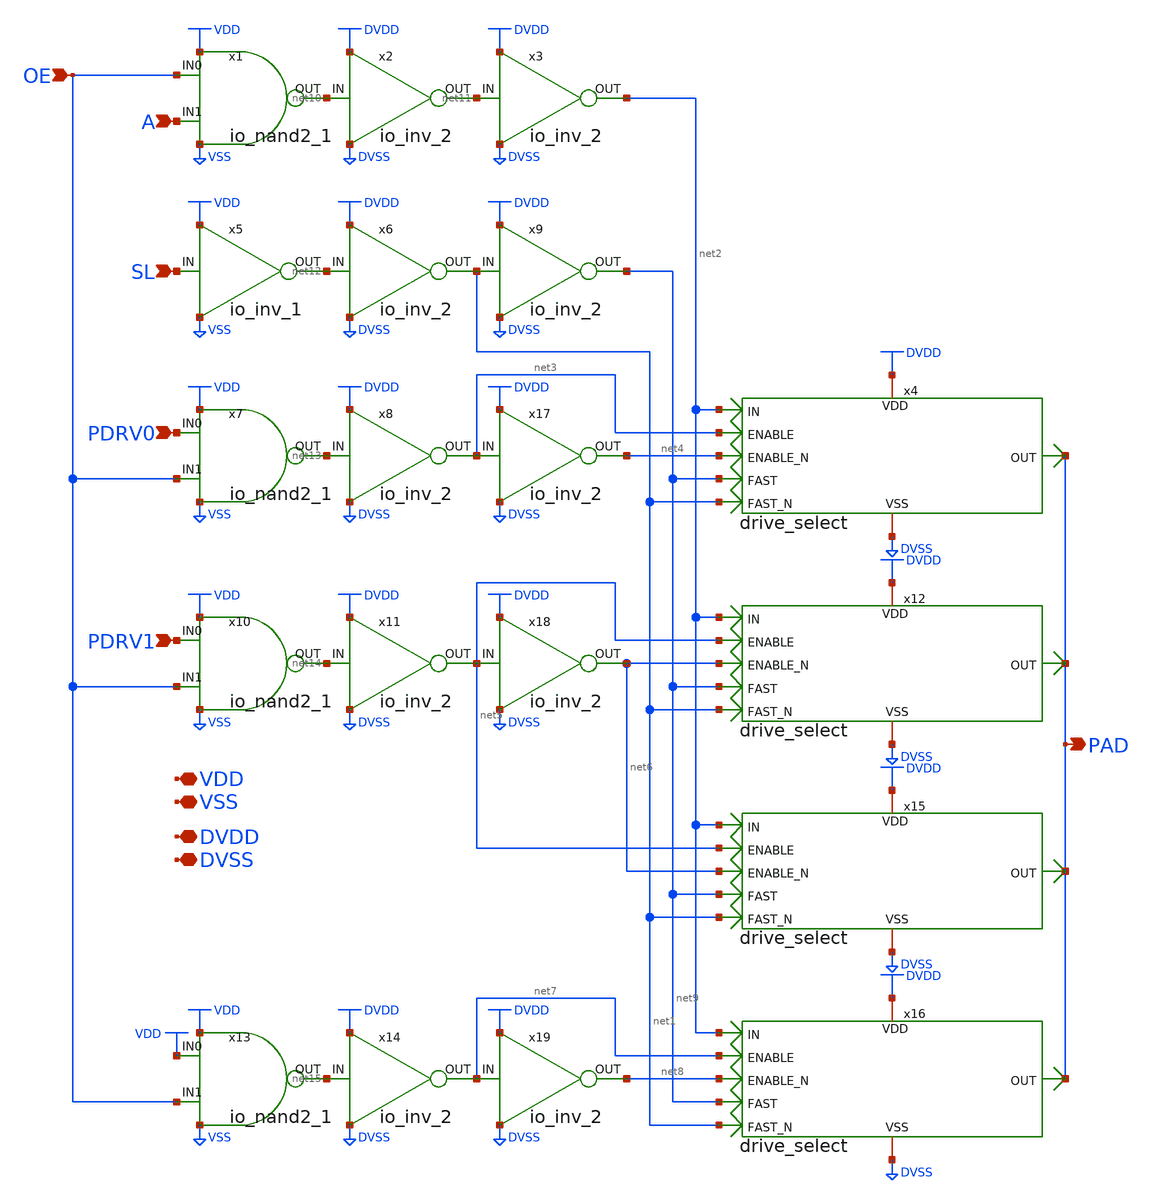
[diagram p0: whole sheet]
** sch_path: io_out.sch
**.subckt io_out OE VDD PAD A SL PDRV0 PDRV1 VSS DVDD DVSS
*.ipin OE
*.iopin VDD
*.opin PAD
*.ipin A
*.ipin SL
*.ipin PDRV0
*.ipin PDRV1
*.iopin VSS
*.iopin DVDD
*.iopin DVSS
x1 OE net10 A VDD VSS io_nand2_1
x2 net10 net11 DVDD DVSS io_inv_2
x3 net11 net2 DVDD DVSS io_inv_2
x4 net1 net2 net3 PAD net9 DVDD DVSS net4 drive_select
x5 SL net12 VDD VSS io_inv_1
x6 net12 net1 DVDD DVSS io_inv_2
x7 PDRV0 net13 OE VDD VSS io_nand2_1
x8 net13 net3 DVDD DVSS io_inv_2
x10 PDRV1 net14 OE VDD VSS io_nand2_1
x11 net14 net5 DVDD DVSS io_inv_2
x13 VDD net15 OE VDD VSS io_nand2_1
x14 net15 net7 DVDD DVSS io_inv_2
x9 net1 net9 DVDD DVSS io_inv_2
x12 net1 net2 net5 PAD net9 DVDD DVSS net6 drive_select
x15 net1 net2 net5 PAD net9 DVDD DVSS net6 drive_select
x16 net1 net2 net7 PAD net9 DVDD DVSS net8 drive_select
x17 net3 net4 DVDD DVSS io_inv_2
x18 net5 net6 DVDD DVSS io_inv_2
x19 net7 net8 DVDD DVSS io_inv_2
**.ends

* expanding   symbol:  io_nand2_1.sym # of pins=5
** sym_path: io_nand2_1.sym
** sch_path: io_nand2_1.sch
.subckt io_nand2_1 IN0 OUT IN1 VDD VSS
*.opin OUT
*.ipin IN0
*.ipin IN1
*.iopin VDD
*.iopin VSS
XM1 OUT IN1 VDD VDD pfet_06v0 L=0.70u W=3u nf=1 ad='int((nf+1)/2) * W/nf * 0.18u' as='int((nf+2)/2) * W/nf * 0.18u'
+ pd='2*int((nf+1)/2) * (W/nf + 0.18u)' ps='2*int((nf+2)/2) * (W/nf + 0.18u)' nrd='0.18u / W' nrs='0.18u / W'
+ sa=0 sb=0 sd=0 m=1
XM2 net1 IN0 VSS VSS nfet_06v0 L=0.70u W=3u nf=1 ad='int((nf+1)/2) * W/nf * 0.18u' as='int((nf+2)/2) * W/nf * 0.18u'
+ pd='2*int((nf+1)/2) * (W/nf + 0.18u)' ps='2*int((nf+2)/2) * (W/nf + 0.18u)' nrd='0.18u / W' nrs='0.18u / W'
+ sa=0 sb=0 sd=0 m=1
XM3 OUT IN1 net1 VSS nfet_06v0 L=0.70u W=3u nf=1 ad='int((nf+1)/2) * W/nf * 0.18u' as='int((nf+2)/2) * W/nf * 0.18u'
+ pd='2*int((nf+1)/2) * (W/nf + 0.18u)' ps='2*int((nf+2)/2) * (W/nf + 0.18u)' nrd='0.18u / W' nrs='0.18u / W'
+ sa=0 sb=0 sd=0 m=1
XM4 OUT IN0 VDD VDD pfet_06v0 L=0.70u W=3u nf=1 ad='int((nf+1)/2) * W/nf * 0.18u' as='int((nf+2)/2) * W/nf * 0.18u'
+ pd='2*int((nf+1)/2) * (W/nf + 0.18u)' ps='2*int((nf+2)/2) * (W/nf + 0.18u)' nrd='0.18u / W' nrs='0.18u / W'
+ sa=0 sb=0 sd=0 m=1
.ends


* expanding   symbol:  io_inv_2.sym # of pins=4
** sym_path: io_inv_2.sym
** sch_path: io_inv_2.sch
.subckt io_inv_2 IN OUT VDD VSS
*.opin OUT
*.ipin IN
*.iopin VDD
*.iopin VSS
XM1 OUT IN VDD VDD pfet_06v0 L=0.70u W=6u nf=1 ad='int((nf+1)/2) * W/nf * 0.18u' as='int((nf+2)/2) * W/nf * 0.18u'
+ pd='2*int((nf+1)/2) * (W/nf + 0.18u)' ps='2*int((nf+2)/2) * (W/nf + 0.18u)' nrd='0.18u / W' nrs='0.18u / W'
+ sa=0 sb=0 sd=0 m=1
XM3 OUT IN VSS VSS nfet_06v0 L=0.70u W=3u nf=1 ad='int((nf+1)/2) * W/nf * 0.18u' as='int((nf+2)/2) * W/nf * 0.18u'
+ pd='2*int((nf+1)/2) * (W/nf + 0.18u)' ps='2*int((nf+2)/2) * (W/nf + 0.18u)' nrd='0.18u / W' nrs='0.18u / W'
+ sa=0 sb=0 sd=0 m=1
.ends


* expanding   symbol:  drive_select.sym # of pins=8
** sym_path: drive_select.sym
** sch_path: drive_select.sch
.subckt drive_select FAST_N IN ENABLE OUT FAST VDD VSS ENABLE_N
*.ipin IN
*.ipin ENABLE
*.ipin FAST
*.ipin FAST_N
*.opin OUT
*.iopin VDD
*.iopin VSS
*.ipin ENABLE_N
XI121 net1 ENABLE VDD VDD pfet_06v0 L=0.70u W=12u nf=1 ad='int((nf+1)/2) * W/nf * 0.18u' as='int((nf+2)/2) * W/nf * 0.18u'
+ pd='2*int((nf+1)/2) * (W/nf + 0.18u)' ps='2*int((nf+2)/2) * (W/nf + 0.18u)' nrd='0.18u / W' nrs='0.18u / W'
+ sa=0 sb=0 sd=0 m=1
XI125 net1 IN VDD VDD pfet_06v0 L=0.70u W=12u nf=1 ad='int((nf+1)/2) * W/nf * 0.18u' as='int((nf+2)/2) * W/nf * 0.18u'
+ pd='2*int((nf+1)/2) * (W/nf + 0.18u)' ps='2*int((nf+2)/2) * (W/nf + 0.18u)' nrd='0.18u / W' nrs='0.18u / W'
+ sa=0 sb=0 sd=0 m=1
XI126 net3 ENABLE_N net1 VDD pfet_06v0 L=0.70u W=12u nf=1 ad='int((nf+1)/2) * W/nf * 0.18u' as='int((nf+2)/2) * W/nf * 0.18u'
+ pd='2*int((nf+1)/2) * (W/nf + 0.18u)' ps='2*int((nf+2)/2) * (W/nf + 0.18u)' nrd='0.18u / W' nrs='0.18u / W'
+ sa=0 sb=0 sd=0 m=1
XI119 net1 ENABLE net3 VSS nfet_06v0 L=0.70u W=6u nf=1 ad='int((nf+1)/2) * W/nf * 0.18u' as='int((nf+2)/2) * W/nf * 0.18u'
+ pd='2*int((nf+1)/2) * (W/nf + 0.18u)' ps='2*int((nf+2)/2) * (W/nf + 0.18u)' nrd='0.18u / W' nrs='0.18u / W'
+ sa=0 sb=0 sd=0 m=1
XI117 net3 IN VSS VSS nfet_06v0 L=0.70u W=6u nf=1 ad='int((nf+1)/2) * W/nf * 0.18u' as='int((nf+2)/2) * W/nf * 0.18u'
+ pd='2*int((nf+1)/2) * (W/nf + 0.18u)' ps='2*int((nf+2)/2) * (W/nf + 0.18u)' nrd='0.18u / W' nrs='0.18u / W'
+ sa=0 sb=0 sd=0 m=1
XI118 net3 ENABLE_N VSS VSS nfet_06v0 L=0.70u W=6u nf=1 ad='int((nf+1)/2) * W/nf * 0.18u' as='int((nf+2)/2) * W/nf * 0.18u'
+ pd='2*int((nf+1)/2) * (W/nf + 0.18u)' ps='2*int((nf+2)/2) * (W/nf + 0.18u)' nrd='0.18u / W' nrs='0.18u / W'
+ sa=0 sb=0 sd=0 m=1
x2 net1 net5 VDD VSS io_inv_4
XI120 net5 FAST_N net2 VDD pfet_06v0 L=0.7u W=24u nf=1 ad='int((nf+1)/2) * W/nf * 0.18u' as='int((nf+2)/2) * W/nf * 0.18u'
+ pd='2*int((nf+1)/2) * (W/nf + 0.18u)' ps='2*int((nf+2)/2) * (W/nf + 0.18u)' nrd='0.18u / W' nrs='0.18u / W'
+ sa=0 sb=0 sd=0 m=1
Xx20 OUT net2 VSS VSS nfet_06v0_dss L=1.15u W=38u nf=1 ad='int((nf+1)/2) * W/nf * 0.18u' as='int((nf+2)/2) * W/nf * 0.18u'
+ pd='2*int((nf+1)/2) * (W/nf + 0.18u)' ps='2*int((nf+2)/2) * (W/nf + 0.18u)' nrd='0.18u / W' nrs='0.18u / W'
+ sa=0 sb=0 sd=0 m=1
XI114 net2 net1 VSS VSS nfet_06v0 L=0.70u W=12u nf=1 ad='int((nf+1)/2) * W/nf * 0.18u' as='int((nf+2)/2) * W/nf * 0.18u'
+ pd='2*int((nf+1)/2) * (W/nf + 0.18u)' ps='2*int((nf+2)/2) * (W/nf + 0.18u)' nrd='0.18u / W' nrs='0.18u / W'
+ sa=0 sb=0 sd=0 m=1
XI124 net2 VSS net5 VDD pfet_06v0 L=0.7u W=1.2u nf=1 ad='int((nf+1)/2) * W/nf * 0.18u' as='int((nf+2)/2) * W/nf * 0.18u'
+ pd='2*int((nf+1)/2) * (W/nf + 0.18u)' ps='2*int((nf+2)/2) * (W/nf + 0.18u)' nrd='0.18u / W' nrs='0.18u / W'
+ sa=0 sb=0 sd=0 m=1
Xx19 OUT net5 VSS VSS nfet_06v0_dss L=1.15u W=38u nf=1 ad='int((nf+1)/2) * W/nf * 0.18u' as='int((nf+2)/2) * W/nf * 0.18u'
+ pd='2*int((nf+1)/2) * (W/nf + 0.18u)' ps='2*int((nf+2)/2) * (W/nf + 0.18u)' nrd='0.18u / W' nrs='0.18u / W'
+ sa=0 sb=0 sd=0 m=1
x3 net3 net4 VDD VSS io_inv_4
XI113 net6 VDD net4 VSS nfet_06v0 L=0.7u W=01.2u nf=1 ad='int((nf+1)/2) * W/nf * 0.18u' as='int((nf+2)/2) * W/nf * 0.18u'
+ pd='2*int((nf+1)/2) * (W/nf + 0.18u)' ps='2*int((nf+2)/2) * (W/nf + 0.18u)' nrd='0.18u / W' nrs='0.18u / W'
+ sa=0 sb=0 sd=0 m=1
XM18 OUT net6 VDD VDD pfet_06v0_dss L=0.7u W=80u nf=1 ad='int((nf+1)/2) * W/nf * 0.18u' as='int((nf+2)/2) * W/nf * 0.18u'
+ pd='2*int((nf+1)/2) * (W/nf + 0.18u)' ps='2*int((nf+2)/2) * (W/nf + 0.18u)' nrd='0.18u / W' nrs='0.18u / W'
+ sa=0 sb=0 sd=0 m=1
XI127 net6 net3 VDD VDD pfet_06v0 L=0.7u W=024u nf=1 ad='int((nf+1)/2) * W/nf * 0.18u' as='int((nf+2)/2) * W/nf * 0.18u'
+ pd='2*int((nf+1)/2) * (W/nf + 0.18u)' ps='2*int((nf+2)/2) * (W/nf + 0.18u)' nrd='0.18u / W' nrs='0.18u / W'
+ sa=0 sb=0 sd=0 m=1
XM21 OUT net4 VDD VDD pfet_06v0_dss L=0.7u W=40u nf=1 ad='int((nf+1)/2) * W/nf * 0.18u' as='int((nf+2)/2) * W/nf * 0.18u'
+ pd='2*int((nf+1)/2) * (W/nf + 0.18u)' ps='2*int((nf+2)/2) * (W/nf + 0.18u)' nrd='0.18u / W' nrs='0.18u / W'
+ sa=0 sb=0 sd=0 m=1
XI112 net4 FAST net6 VSS nfet_06v0 L=0.7u W=12u nf=1 ad='int((nf+1)/2) * W/nf * 0.18u' as='int((nf+2)/2) * W/nf * 0.18u'
+ pd='2*int((nf+1)/2) * (W/nf + 0.18u)' ps='2*int((nf+2)/2) * (W/nf + 0.18u)' nrd='0.18u / W' nrs='0.18u / W'
+ sa=0 sb=0 sd=0 m=1
.ends


* expanding   symbol:  io_inv_4.sym # of pins=4
** sym_path: io_inv_4.sym
** sch_path: io_inv_4.sch
.subckt io_inv_4 IN OUT VDD VSS
*.opin OUT
*.ipin IN
*.iopin VDD
*.iopin VSS
XM1 OUT IN VDD VDD pfet_06v0 L=0.70u W=24u nf=1 ad='int((nf+1)/2) * W/nf * 0.18u' as='int((nf+2)/2) * W/nf * 0.18u'
+ pd='2*int((nf+1)/2) * (W/nf + 0.18u)' ps='2*int((nf+2)/2) * (W/nf + 0.18u)' nrd='0.18u / W' nrs='0.18u / W'
+ sa=0 sb=0 sd=0 m=1
XM3 OUT IN VSS VSS nfet_06v0 L=0.70u W=12u nf=1 ad='int((nf+1)/2) * W/nf * 0.18u' as='int((nf+2)/2) * W/nf * 0.18u'
+ pd='2*int((nf+1)/2) * (W/nf + 0.18u)' ps='2*int((nf+2)/2) * (W/nf + 0.18u)' nrd='0.18u / W' nrs='0.18u / W'
+ sa=0 sb=0 sd=0 m=1
.ends

.GLOBAL VDD
.GLOBAL DVDD
.end
